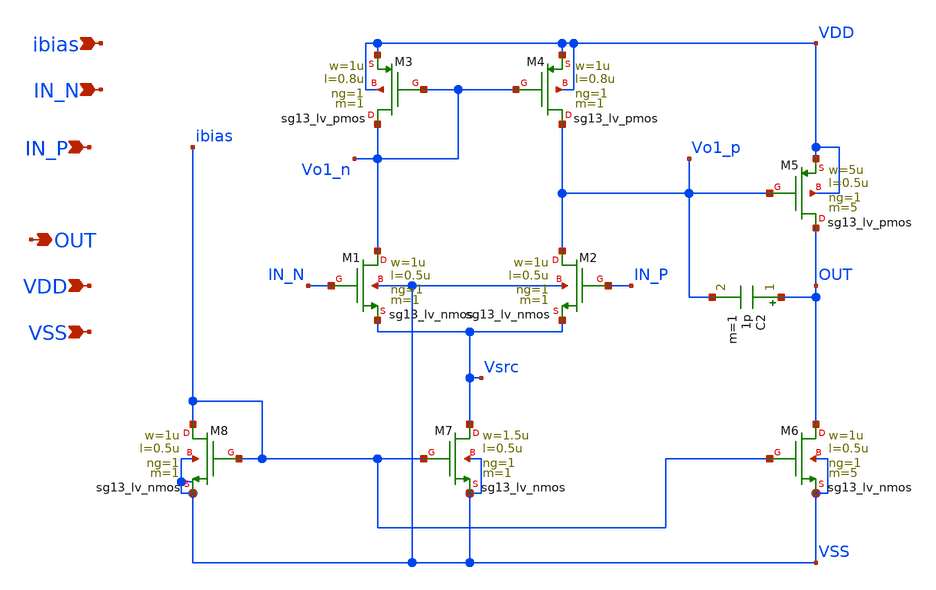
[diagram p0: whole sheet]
** sch_path: xschem/Tareas/Tarea_2/OTA3.sch
**.subckt OTA3 IN_N IN_P OUT VDD VSS ibias
*.ipin IN_N
*.ipin IN_P
*.opin OUT
*.ipin VDD
*.ipin VSS
*.ipin ibias
C2 OUT Vo1_p 1p m=1
XM8 ibias ibias VSS VSS sg13_lv_nmos w=1u l=0.5u ng=1 m=1 mm_ok=1
XM7 Vsrc ibias VSS VSS sg13_lv_nmos w=1.5u l=0.5u ng=1 m=1 mm_ok=1
XM6 OUT ibias VSS VSS sg13_lv_nmos w=1u l=0.5u ng=1 m=5 mm_ok=1
XM1 Vo1_n IN_N Vsrc VSS sg13_lv_nmos w=1u l=0.5u ng=1 m=1 mm_ok=1
XM2 Vo1_p IN_P Vsrc VSS sg13_lv_nmos w=1u l=0.5u ng=1 m=1 mm_ok=1
XM3 Vo1_n Vo1_n VDD VDD sg13_lv_pmos w=1u l=0.8u ng=1 m=1 mm_ok=1
XM4 Vo1_p Vo1_n VDD VDD sg13_lv_pmos w=1u l=0.8u ng=1 m=1 mm_ok=1
XM5 OUT Vo1_p VDD VDD sg13_lv_pmos w=5u l=0.5u ng=1 m=5 mm_ok=1
**.ends
.end
